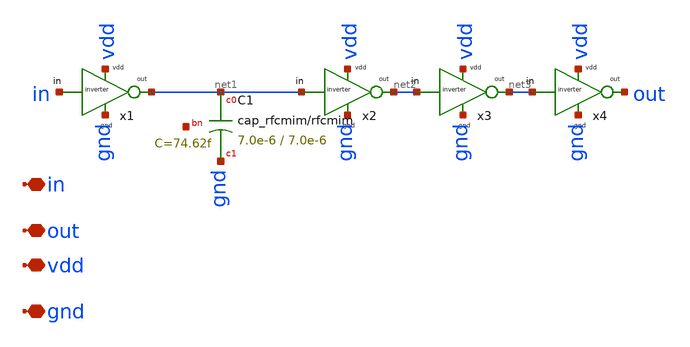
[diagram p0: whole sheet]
** sch_path: Clock_gen_using_transistor_hv/buffer.sch
**.subckt buffer in out vdd gnd
*.iopin in
*.iopin out
*.iopin vdd
*.iopin gnd
x1 in net1 vdd gnd inverter
x2 net1 net2 vdd gnd inverter
x3 net2 net3 vdd gnd inverter
x4 net3 out vdd gnd inverter
XC1 net1 gnd net4 cap_rfcmim w=7.0e-6 l=7.0e-6 wfeed=5.0e-6 m=1 mm_ok=1
**.ends

* expanding   symbol:
*+  /home/designer/shared/unicass_2026/Design_Files/github_clone_circuit_/UNI-CASS_Project_2025_IIT_DH/Clock_gen_using_transistor_hv/inverter.sym # of pins=4
** sym_path: /home/designer/shared/unicass_2026/Design_Files/github_clone_circuit_/UNI-CASS_Project_2025_IIT_DH/Clock_gen_using_transistor_hv/inverter.sym
** sch_path: /home/designer/shared/unicass_2026/Design_Files/github_clone_circuit_/UNI-CASS_Project_2025_IIT_DH/Clock_gen_using_transistor_hv/inverter.sch
.subckt inverter in out vdd gnd
*.iopin in
*.iopin vdd
*.iopin out
*.iopin gnd
XM3 out in vdd vdd sg13_hv_pmos w=2u l=2u ng=1 m=1 mm_ok=1
XM1 out in gnd gnd sg13_hv_nmos w=1u l=1u ng=1 m=1 mm_ok=1
.ends

.end
